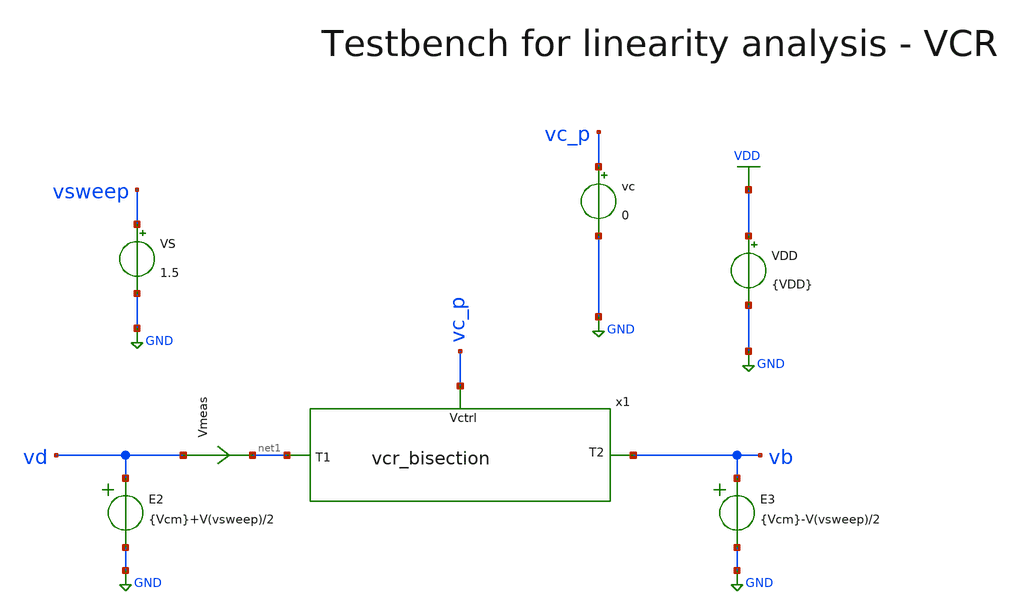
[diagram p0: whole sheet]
** sch_path: macros/macros/vcr_bisection/testbenches/xschem/res_tb_linearity.sch
**.subckt res_tb_linearity
VDD VDD GND {VDD}
VS vsweep GND 1.5
Vmeas vd net1 0
.save i(vmeas)
E2 vd GND VOL=' {Vcm}+V(vsweep)/2 '
E3 vb GND VOL=' {Vcm}-V(vsweep)/2 '
vc vc_p GND 0
x1 vc_p net1 vb vcr_bisection
**** begin user architecture code

.lib cornerMOSlv.lib mos_tt
.lib cornerMOShv.lib mos_tt
.lib cornerRES.lib res_typ
.lib cornerDIO.lib dio_tt



* .include ../../../netlist/pex/inverter_magic_pex_3.spice
.param VDD=3.3
.csparam VDD=VDD
.param Vcm=2
.csparam Vcm=Vcm
.param temp=27
.options savecurrents klu method=gear reltol=1e-3 abstol=1e-15 gmin=1e-15
.control
let vcc = 0

save all
set appendwrite



repeat 5
  alter vc $&vcc

  * DC Sweep
  dc VS -1 1 1m
  remzerovec
  let vcc = vcc + 0.2
end
write @schname\.raw
set appendwrite

* Plotting
plot dc1.v(vsweep)/(dc1.v.x1.Vmeas#branch) dc2.v(vsweep)/(dc2.v.x1.Vmeas#branch)
+ dc3.v(vsweep)/(dc3.v.x1.Vmeas#branch) dc4.v(vsweep)/(dc4.v.x1.Vmeas#branch) dc5.v(vsweep)/(dc5.v.x1.Vmeas#branch) ylimit 0 10k

plot dc1.v.x1.Vmeas#branch dc2.v.x1.Vmeas#branch dc3.v.x1.Vmeas#branch dc4.v.x1.Vmeas#branch
+ dc5.v.x1.Vmeas#branch

* Write Data
unset appendwrite
set wr_vecnames
set wr_singlescale
wrdata ../plot_simulations/data/@schname\.txt v(vc_p) dc1.v(vsweep)/(dc1.i(Vmeas))
+ dc2.v(vsweep)/(dc2.i(Vmeas)) dc3.v(vsweep)/(dc3.i(Vmeas)) dc4.v(vsweep)/(dc4.i(Vmeas)) dc5.v(vsweep)/(dc5.i(Vmeas))

write res_tb_linearity.raw

*quit
.endc


**** end user architecture code
**.ends

* expanding   symbol:
*+  /home/santi/heichips26-voltage-controlled-resistor/macros/vcr_bisection/schematic/xschem/vcr_bisection.sym # of pins=3
** sym_path: macros/heichips26_analog_project/macros/vcr_bisection/schematic/xschem/vcr_bisection.sym
** sch_path: macros/heichips26_analog_project/macros/vcr_bisection/schematic/xschem/vcr_bisection.sch
.subckt vcr_bisection Vctrl T1 T2
*.ipin T1
*.ipin T2
*.ipin Vctrl
R1 vcm T1 10k m=1
R2 T2 vcm 10k m=1
Vmeas T1 net1 0
.save i(vmeas)
XM1 net1 Vctrl T2 vcm sg13_hv_pmos w=50u l=10u ng=10 m=1 mm_ok=1
.ends

.GLOBAL GND
.GLOBAL VDD
.end
